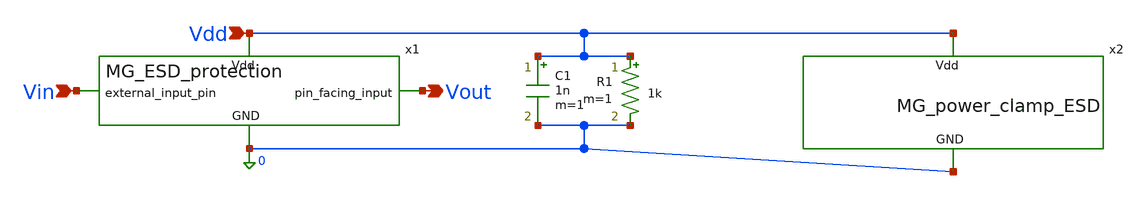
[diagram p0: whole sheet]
** sch_path: MG_ESD_protection/MG_ESD_protection_testbench.sch
**.subckt MG_ESD_protection_testbench Vin Vdd Vout
*.ipin Vin
*.ipin Vdd
*.opin Vout
x1 Vdd Vin Vout 0 MG_ESD_protection
C1 Vdd 0 1n m=1
R1 Vdd 0 1k m=1
x2 Vdd 0 MG_power_clamp_ESD
**** begin user architecture code


* --- 1. GF180MCU PDK Libraries --
.include /foss/pdks/gf180mcuD/libs.tech/ngspice/design.ngspice
.lib /foss/pdks/gf180mcuD/libs.tech/ngspice/sm141064.ngspice typical
.lib /foss/pdks/gf180mcuD/libs.tech/ngspice/sm141064.ngspice res_typical
.lib /foss/pdks/gf180mcuD/libs.tech/ngspice/sm141064.ngspice mimcap_typical
.lib /foss/pdks/gf180mcuD/libs.tech/ngspice/sm141064.ngspice cap_mim
.lib /foss/pdks/gf180mcuD/libs.tech/ngspice/sm141064.ngspice diode_typical

* --- 2. Chip Power Supply ---
* Vdd is grounded for testing (chip is OFF)
V1 Vdd 0 0.0

* --- 3. 2kV HBM Strike Generator ---
* A 100pF capacitor charged to 2000 Volts (ic=2000)
C_HBM hbm_node 0 100p ic=2000
* A 1.5k resistor discharging the capacitor directly into your 'Vin' pad
R_HBM hbm_node Vin 1.5k

* --- 4. Internal Logic Dummy Load ---
* A 50fF capacitor on Vout to simulate the gate capacitance of your decoder
C_load Vout 0 50f

* --- 5. Simulation Control ---
.options method=gear reltol=1e-4

.control
* Run a 1us transient simulation.
* 'uic' is REQUIRED to apply the 2000V initial condition to the capacitor.
tran 0.1n 1u uic

* Plot 1: See the raw 2000V spike discharging
plot v(hbm_node) title 'Raw 2kV HBM Spike'

* Plot 2: Verify the protection.
* v(Vin) should be clamped to a few volts safely above Vdd or below GND.
* v(Vout) is the safe voltage your logic gates will actually see.
plot v(Vin) v(Vout) title 'Clamped Voltage at Pad and Logic'
.endc


**** end user architecture code
**.ends
.end
